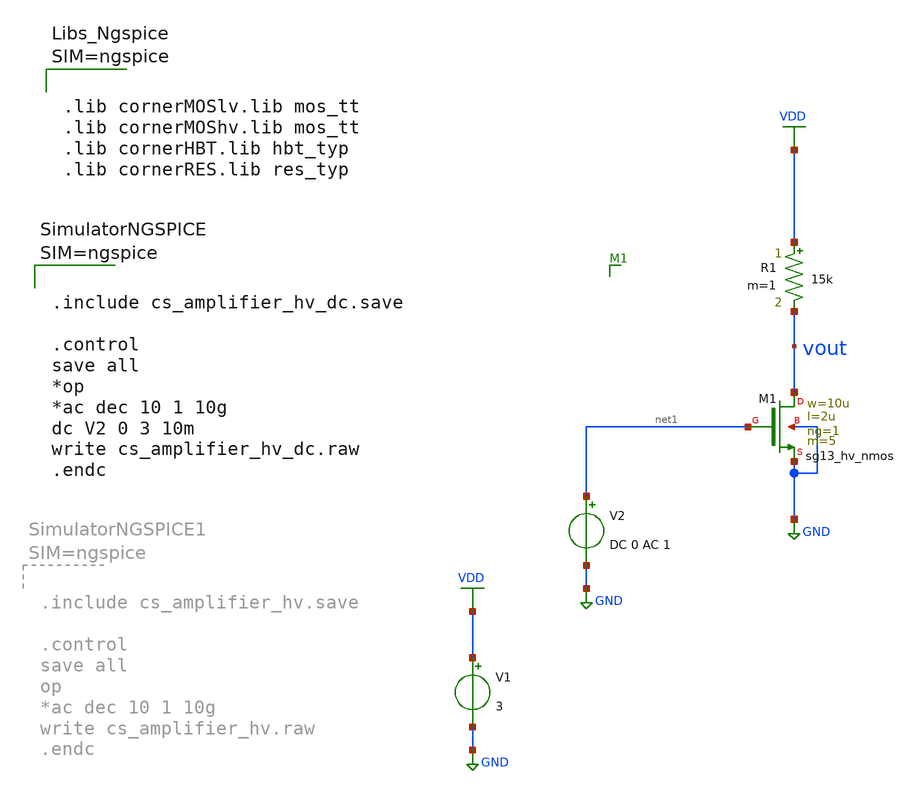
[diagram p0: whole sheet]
** sch_path: Schematics/lab_1/cs_amplifier_hv_dc.sch
**.subckt cs_amplifier_hv_dc
R1 VDD vout 15k m=1
V1 VDD GND 3
V2 net1 GND DC 0 AC 1
XM1 vout net1 GND GND sg13_hv_nmos w=10u l=2u ng=1 m=5 mm_ok=1
**** begin user architecture code



.lib cornerMOSlv.lib mos_tt
.lib cornerMOShv.lib mos_tt
.lib cornerHBT.lib hbt_typ
.lib cornerRES.lib res_typ






.include cs_amplifier_hv_dc.save

.control
save all
*op
*ac dec 10 1 10g
dc V2 0 3 10m
write cs_amplifier_hv_dc.raw
.endc



**** end user architecture code
**.ends
.GLOBAL GND
.GLOBAL VDD
.end
